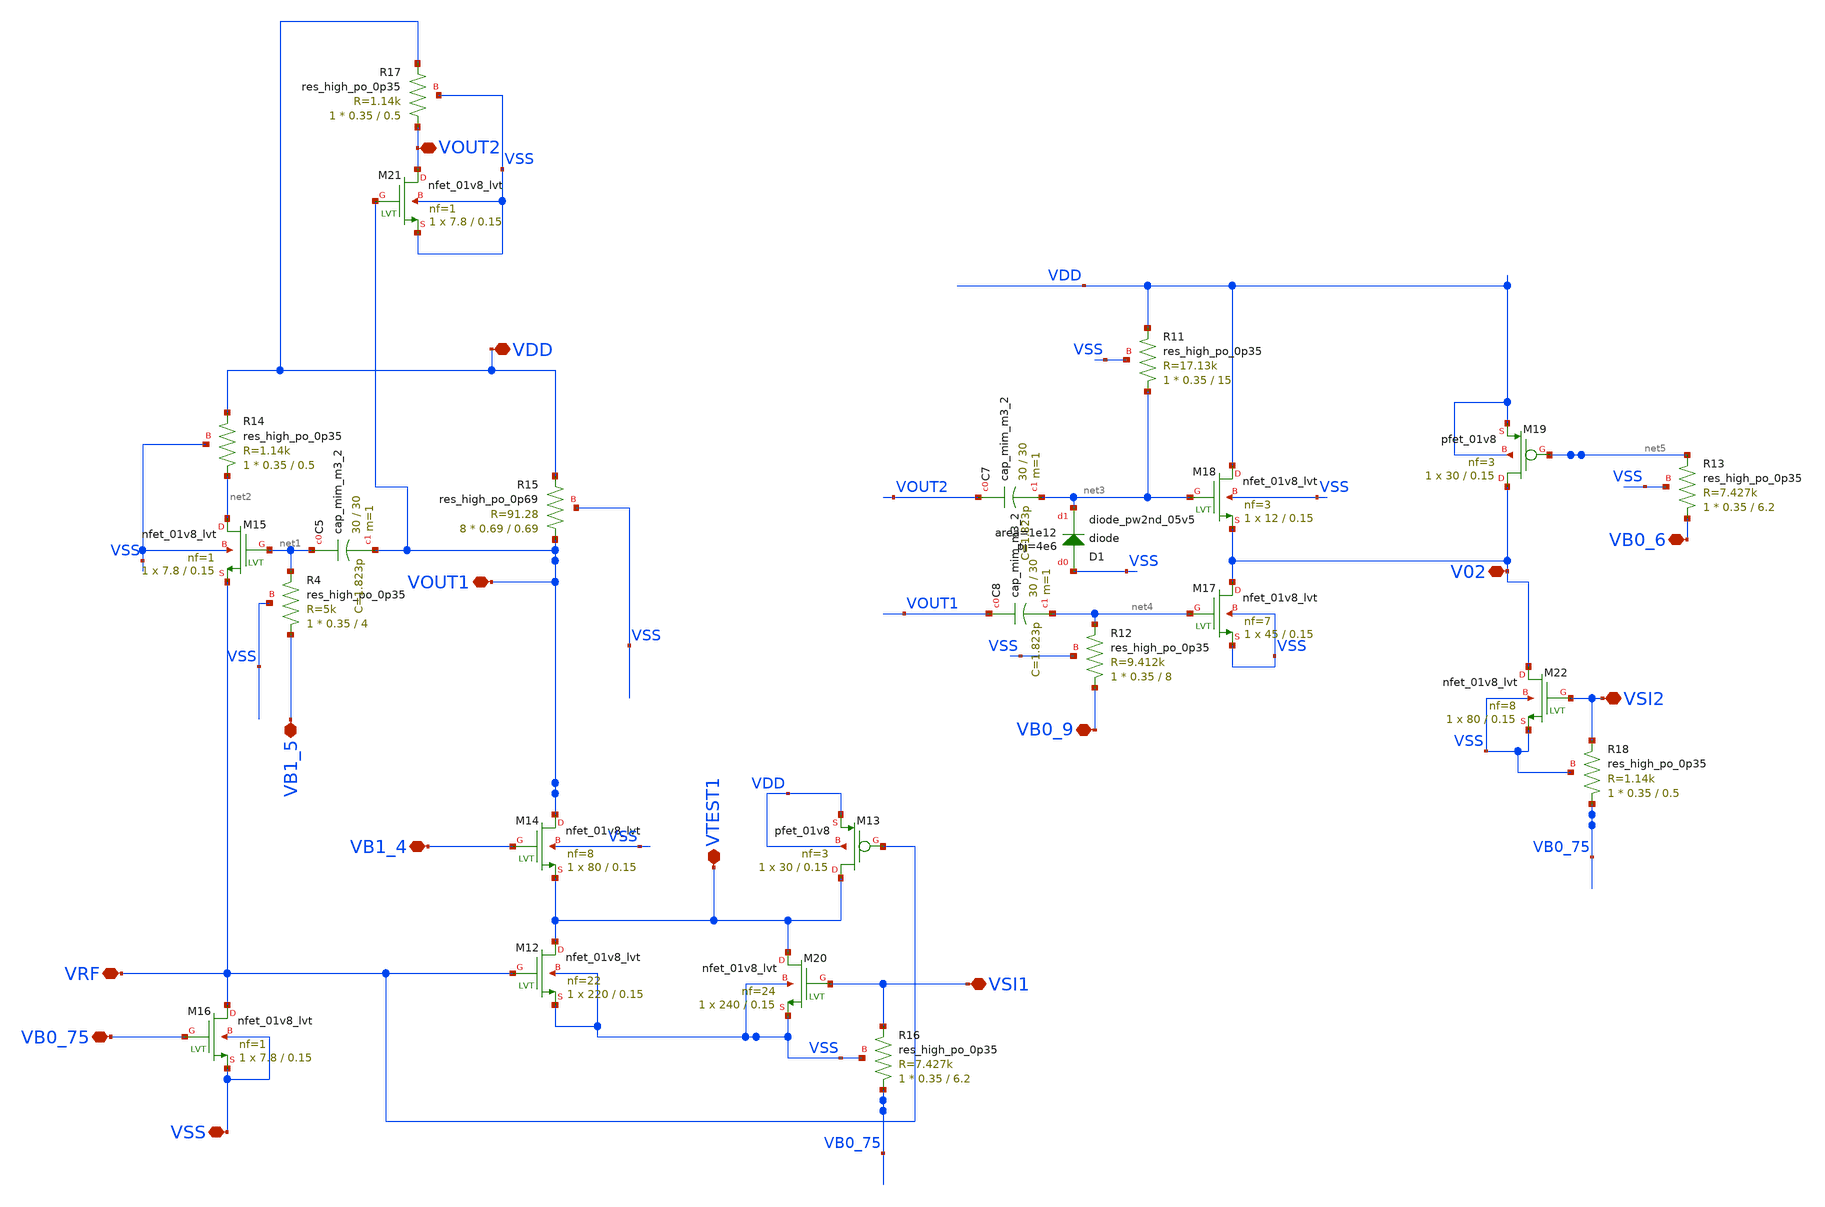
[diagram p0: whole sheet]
** sch_path: xschem/xschem4_sic_oct_20/partitions4_individual.sch
**.subckt partitions4_individual VRF VSS VB0_75 VSI1 VB1_4 VTEST1 VDD VOUT1 VOUT2 VB1_5 VB0_9 VSI2
*+ VB0_6 V02
*.iopin VRF
*.iopin VSS
*.iopin VB0_75
*.iopin VSI1
*.iopin VB1_4
*.iopin VTEST1
*.iopin VDD
*.iopin VOUT1
*.iopin VOUT2
*.iopin VB1_5
*.iopin VB0_9
*.iopin VSI2
*.iopin VB0_6
*.iopin V02
XM12 VTEST1 VRF VSS VSS sky130_fd_pr__nfet_01v8_lvt L=0.15 W=220 nf=22 ad='int((nf+1)/2) * W/nf * 0.29'
+ as='int((nf+2)/2) * W/nf * 0.29' pd='2*int((nf+1)/2) * (W/nf + 0.29)' ps='2*int((nf+2)/2) * (W/nf + 0.29)'
+ nrd='0.29 / W' nrs='0.29 / W' sa=0 sb=0 sd=0 mult=1 m=1
XM13 VTEST1 VRF VDD VDD sky130_fd_pr__pfet_01v8 L=0.15 W=30 nf=3 ad='int((nf+1)/2) * W/nf * 0.29' as='int((nf+2)/2) * W/nf * 0.29'
+ pd='2*int((nf+1)/2) * (W/nf + 0.29)' ps='2*int((nf+2)/2) * (W/nf + 0.29)' nrd='0.29 / W' nrs='0.29 / W'
+ sa=0 sb=0 sd=0 mult=1 m=1
XM14 VOUT1 VB1_4 VTEST1 VSS sky130_fd_pr__nfet_01v8_lvt L=0.15 W=80 nf=8 ad='int((nf+1)/2) * W/nf * 0.29'
+ as='int((nf+2)/2) * W/nf * 0.29' pd='2*int((nf+1)/2) * (W/nf + 0.29)' ps='2*int((nf+2)/2) * (W/nf + 0.29)'
+ nrd='0.29 / W' nrs='0.29 / W' sa=0 sb=0 sd=0 mult=1 m=1
XM16 VRF VB0_75 VSS VSS sky130_fd_pr__nfet_01v8_lvt L=0.15 W=7.8 nf=1 ad='int((nf+1)/2) * W/nf * 0.29'
+ as='int((nf+2)/2) * W/nf * 0.29' pd='2*int((nf+1)/2) * (W/nf + 0.29)' ps='2*int((nf+2)/2) * (W/nf + 0.29)'
+ nrd='0.29 / W' nrs='0.29 / W' sa=0 sb=0 sd=0 mult=1 m=1
XM20 VTEST1 VSI1 VSS VSS sky130_fd_pr__nfet_01v8_lvt L=0.15 W=240 nf=24 ad='int((nf+1)/2) * W/nf * 0.29'
+ as='int((nf+2)/2) * W/nf * 0.29' pd='2*int((nf+1)/2) * (W/nf + 0.29)' ps='2*int((nf+2)/2) * (W/nf + 0.29)'
+ nrd='0.29 / W' nrs='0.29 / W' sa=0 sb=0 sd=0 mult=1 m=1
XR16 VB0_75 VSI1 VSS sky130_fd_pr__res_high_po_0p35 L=6.2 mult=1 m=1
XR4 VB1_5 net1 VSS sky130_fd_pr__res_high_po_0p35 L=4 mult=1 m=1
XC5 net1 VOUT1 sky130_fd_pr__cap_mim_m3_2 W=30 L=30 MF=1 m=1
XM15 net2 net1 VRF VSS sky130_fd_pr__nfet_01v8_lvt L=0.15 W=7.8 nf=1 ad='int((nf+1)/2) * W/nf * 0.29'
+ as='int((nf+2)/2) * W/nf * 0.29' pd='2*int((nf+1)/2) * (W/nf + 0.29)' ps='2*int((nf+2)/2) * (W/nf + 0.29)'
+ nrd='0.29 / W' nrs='0.29 / W' sa=0 sb=0 sd=0 mult=1 m=1
XR14 net2 VDD VSS sky130_fd_pr__res_high_po_0p35 L=0.5 mult=1 m=1
XR15 VOUT1 VDD VSS sky130_fd_pr__res_high_po_0p69 L=0.69 mult=8 m=8
XM21 VOUT2 VOUT1 VSS VSS sky130_fd_pr__nfet_01v8_lvt L=0.15 W=7.8 nf=1 ad='int((nf+1)/2) * W/nf * 0.29'
+ as='int((nf+2)/2) * W/nf * 0.29' pd='2*int((nf+1)/2) * (W/nf + 0.29)' ps='2*int((nf+2)/2) * (W/nf + 0.29)'
+ nrd='0.29 / W' nrs='0.29 / W' sa=0 sb=0 sd=0 mult=1 m=1
XR17 VOUT2 VDD VSS sky130_fd_pr__res_high_po_0p35 L=0.5 mult=1 m=1
XM17 V02 net4 VSS VSS sky130_fd_pr__nfet_01v8_lvt L=0.15 W=45 nf=7 ad='int((nf+1)/2) * W/nf * 0.29' as='int((nf+2)/2) * W/nf * 0.29'
+ pd='2*int((nf+1)/2) * (W/nf + 0.29)' ps='2*int((nf+2)/2) * (W/nf + 0.29)' nrd='0.29 / W' nrs='0.29 / W'
+ sa=0 sb=0 sd=0 mult=1 m=1
XM18 VDD net3 V02 VSS sky130_fd_pr__nfet_01v8_lvt L=0.15 W=12 nf=3 ad='int((nf+1)/2) * W/nf * 0.29' as='int((nf+2)/2) * W/nf * 0.29'
+ pd='2*int((nf+1)/2) * (W/nf + 0.29)' ps='2*int((nf+2)/2) * (W/nf + 0.29)' nrd='0.29 / W' nrs='0.29 / W'
+ sa=0 sb=0 sd=0 mult=1 m=1
XR11 net3 VDD VSS sky130_fd_pr__res_high_po_0p35 L=15 mult=1 m=1
XC7 VOUT2 net3 sky130_fd_pr__cap_mim_m3_2 W=30 L=30 MF=1 m=1
XR12 VB0_9 net4 VSS sky130_fd_pr__res_high_po_0p35 L=8 mult=1 m=1
XC8 VOUT1 net4 sky130_fd_pr__cap_mim_m3_2 W=30 L=30 MF=1 m=1
XD1 VSS net3 sky130_fd_pr__diode_pw2nd_05v5 area=1e12 pj=4e6
XM19 V02 net5 VDD VDD sky130_fd_pr__pfet_01v8 L=0.15 W=30 nf=3 ad='int((nf+1)/2) * W/nf * 0.29' as='int((nf+2)/2) * W/nf * 0.29'
+ pd='2*int((nf+1)/2) * (W/nf + 0.29)' ps='2*int((nf+2)/2) * (W/nf + 0.29)' nrd='0.29 / W' nrs='0.29 / W'
+ sa=0 sb=0 sd=0 mult=1 m=1
XR13 VB0_6 net5 VSS sky130_fd_pr__res_high_po_0p35 L=6.2 mult=1 m=1
XM22 V02 VSI2 VSS VSS sky130_fd_pr__nfet_01v8_lvt L=0.15 W=80 nf=8 ad='int((nf+1)/2) * W/nf * 0.29' as='int((nf+2)/2) * W/nf * 0.29'
+ pd='2*int((nf+1)/2) * (W/nf + 0.29)' ps='2*int((nf+2)/2) * (W/nf + 0.29)' nrd='0.29 / W' nrs='0.29 / W'
+ sa=0 sb=0 sd=0 mult=1 m=1
XR18 VB0_75 VSI2 VSS sky130_fd_pr__res_high_po_0p35 L=0.5 mult=1 m=1
**.ends
.end
